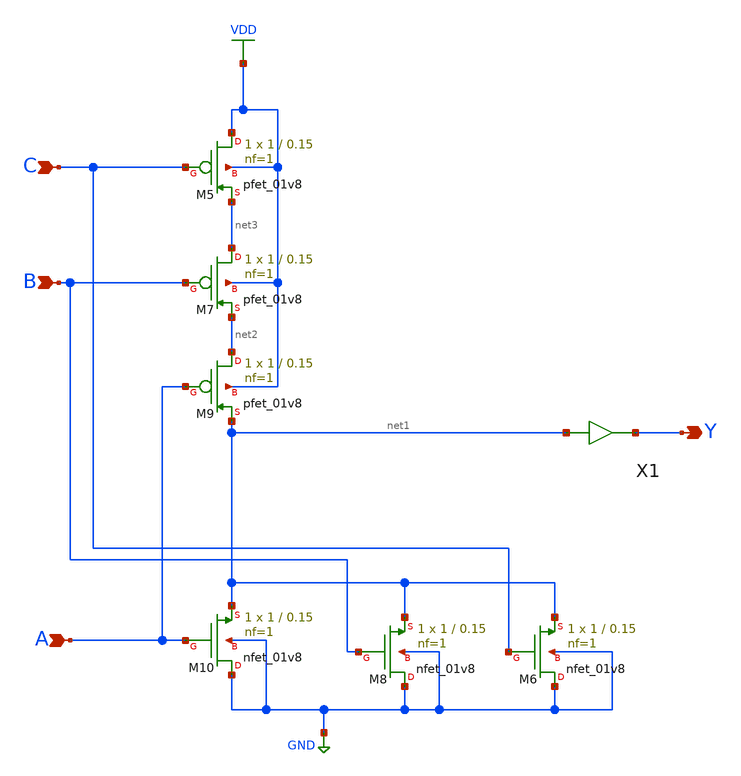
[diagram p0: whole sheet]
** sch_path: gates/OR3.sch
**.subckt OR3 A B Y C
*.ipin A
*.ipin B
*.opin Y
*.ipin C
XM5 VDD C net3 VDD sky130_fd_pr__pfet_01v8 L=0.15 W=1 nf=1 ad='int((nf+1)/2) * W/nf * 0.29' as='int((nf+2)/2) * W/nf * 0.29'
+ pd='2*int((nf+1)/2) * (W/nf + 0.29)' ps='2*int((nf+2)/2) * (W/nf + 0.29)' nrd='0.29 / W' nrs='0.29 / W'
+ sa=0 sb=0 sd=0 mult=1 m=1
XM6 GND C net1 GND sky130_fd_pr__nfet_01v8 L=0.15 W=1 nf=1 ad='int((nf+1)/2) * W/nf * 0.29' as='int((nf+2)/2) * W/nf * 0.29'
+ pd='2*int((nf+1)/2) * (W/nf + 0.29)' ps='2*int((nf+2)/2) * (W/nf + 0.29)' nrd='0.29 / W' nrs='0.29 / W'
+ sa=0 sb=0 sd=0 mult=1 m=1
XM7 net3 B net2 VDD sky130_fd_pr__pfet_01v8 L=0.15 W=1 nf=1 ad='int((nf+1)/2) * W/nf * 0.29' as='int((nf+2)/2) * W/nf * 0.29'
+ pd='2*int((nf+1)/2) * (W/nf + 0.29)' ps='2*int((nf+2)/2) * (W/nf + 0.29)' nrd='0.29 / W' nrs='0.29 / W'
+ sa=0 sb=0 sd=0 mult=1 m=1
XM8 GND B net1 GND sky130_fd_pr__nfet_01v8 L=0.15 W=1 nf=1 ad='int((nf+1)/2) * W/nf * 0.29' as='int((nf+2)/2) * W/nf * 0.29'
+ pd='2*int((nf+1)/2) * (W/nf + 0.29)' ps='2*int((nf+2)/2) * (W/nf + 0.29)' nrd='0.29 / W' nrs='0.29 / W'
+ sa=0 sb=0 sd=0 mult=1 m=1
XM9 net2 A net1 VDD sky130_fd_pr__pfet_01v8 L=0.15 W=1 nf=1 ad='int((nf+1)/2) * W/nf * 0.29' as='int((nf+2)/2) * W/nf * 0.29'
+ pd='2*int((nf+1)/2) * (W/nf + 0.29)' ps='2*int((nf+2)/2) * (W/nf + 0.29)' nrd='0.29 / W' nrs='0.29 / W'
+ sa=0 sb=0 sd=0 mult=1 m=1
XM10 GND A net1 GND sky130_fd_pr__nfet_01v8 L=0.15 W=1 nf=1 ad='int((nf+1)/2) * W/nf * 0.29' as='int((nf+2)/2) * W/nf * 0.29'
+ pd='2*int((nf+1)/2) * (W/nf + 0.29)' ps='2*int((nf+2)/2) * (W/nf + 0.29)' nrd='0.29 / W' nrs='0.29 / W'
+ sa=0 sb=0 sd=0 mult=1 m=1
X1 net1 Y inv_vtc
**.ends

* expanding   symbol:  /home/apn/test_xschem_sky130/inv_vtc.sym # of pins=2
** sym_path: gates/inv_vtc.sym
** sch_path: gates/inv_vtc.sch
.subckt inv_vtc A Y
*.ipin A
*.opin Y
XM1 Y A VDD VDD sky130_fd_pr__pfet_01v8 L=0.15 W=2 nf=1 ad='int((nf+1)/2) * W/nf * 0.29' as='int((nf+2)/2) * W/nf * 0.29'
+ pd='2*int((nf+1)/2) * (W/nf + 0.29)' ps='2*int((nf+2)/2) * (W/nf + 0.29)' nrd='0.29 / W' nrs='0.29 / W'
+ sa=0 sb=0 sd=0 mult=1 m=1
XM2 Y A GND GND sky130_fd_pr__nfet_01v8 L=0.15 W=1 nf=1 ad='int((nf+1)/2) * W/nf * 0.29' as='int((nf+2)/2) * W/nf * 0.29'
+ pd='2*int((nf+1)/2) * (W/nf + 0.29)' ps='2*int((nf+2)/2) * (W/nf + 0.29)' nrd='0.29 / W' nrs='0.29 / W'
+ sa=0 sb=0 sd=0 mult=1 m=1
.ends

.GLOBAL VDD
.GLOBAL GND
.end
